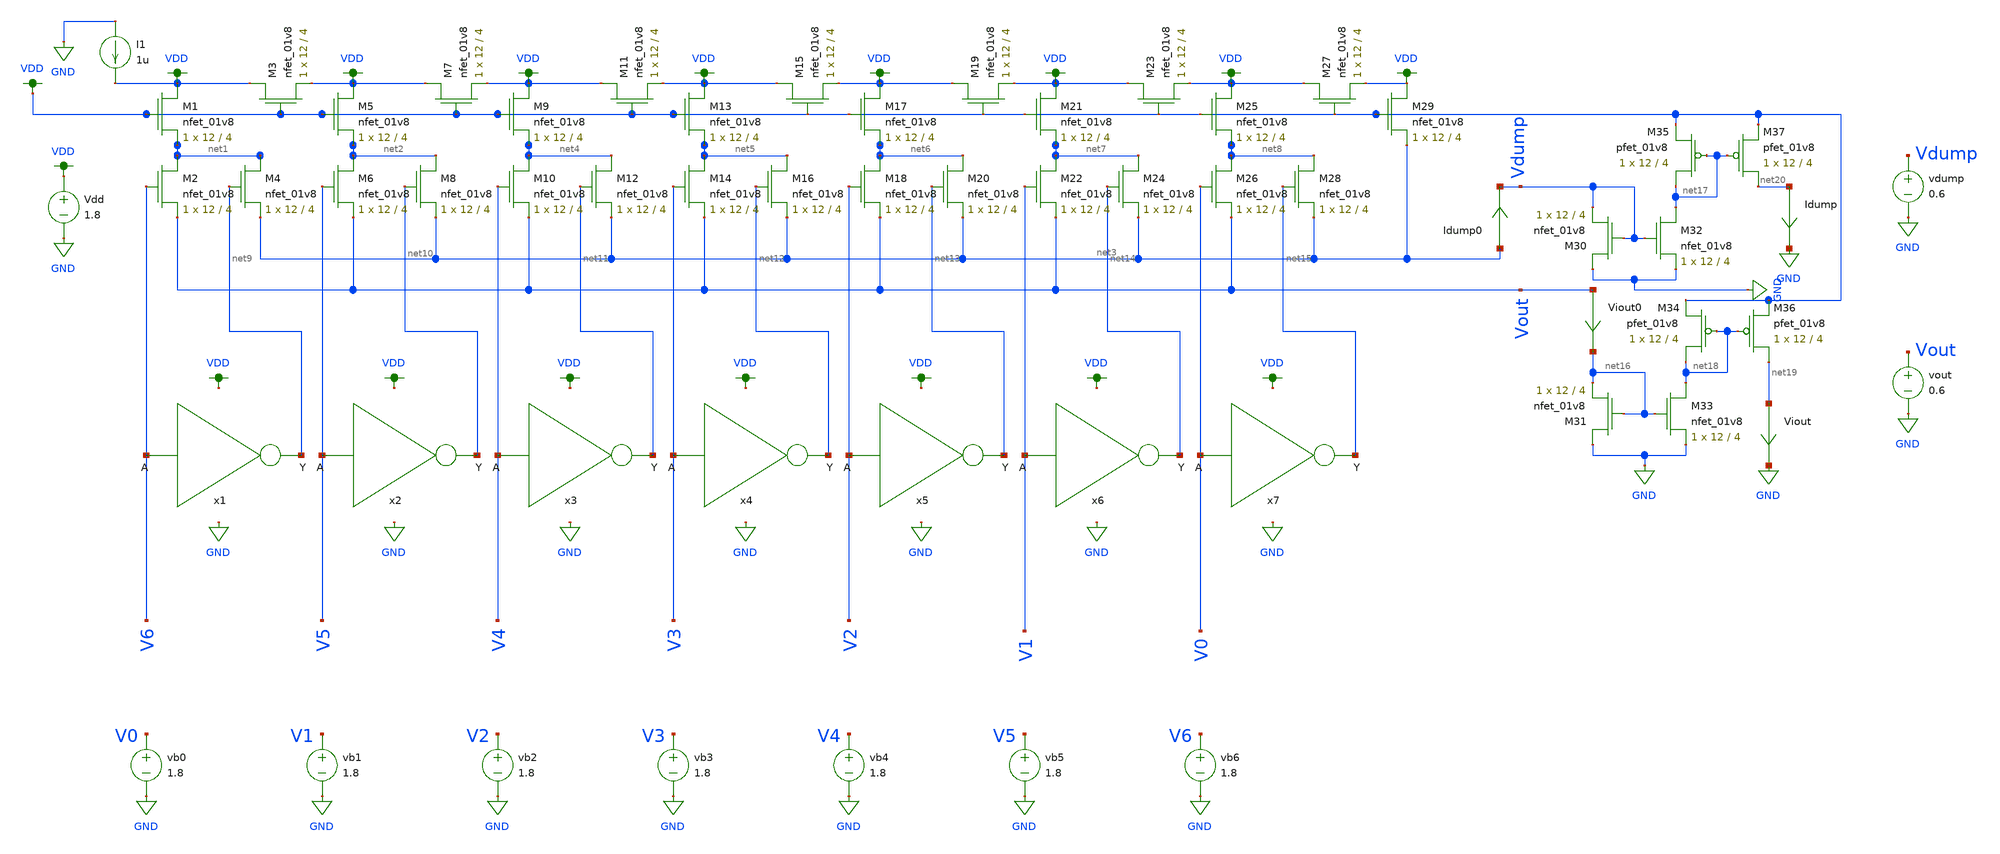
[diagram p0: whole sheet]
** sch_path: xschem/ladder_dac_simulation.sch
**.subckt ladder_dac_simulation
XM1 VDD VDD net1 GND sky130_fd_pr__nfet_01v8 L=4 W=12 nf=1 ad='int((nf+1)/2) * W/nf * 0.29' as='int((nf+2)/2) * W/nf * 0.29'
+ pd='2*int((nf+1)/2) * (W/nf + 0.29)' ps='2*int((nf+2)/2) * (W/nf + 0.29)' nrd='0.29 / W' nrs='0.29 / W'
+ sa=0 sb=0 sd=0 mult=1 m=1
XM3 VDD VDD VDD GND sky130_fd_pr__nfet_01v8 L=4 W=12 nf=1 ad='int((nf+1)/2) * W/nf * 0.29' as='int((nf+2)/2) * W/nf * 0.29'
+ pd='2*int((nf+1)/2) * (W/nf + 0.29)' ps='2*int((nf+2)/2) * (W/nf + 0.29)' nrd='0.29 / W' nrs='0.29 / W'
+ sa=0 sb=0 sd=0 mult=1 m=1
XM5 VDD VDD net2 GND sky130_fd_pr__nfet_01v8 L=4 W=12 nf=1 ad='int((nf+1)/2) * W/nf * 0.29' as='int((nf+2)/2) * W/nf * 0.29'
+ pd='2*int((nf+1)/2) * (W/nf + 0.29)' ps='2*int((nf+2)/2) * (W/nf + 0.29)' nrd='0.29 / W' nrs='0.29 / W'
+ sa=0 sb=0 sd=0 mult=1 m=1
XM7 VDD VDD VDD GND sky130_fd_pr__nfet_01v8 L=4 W=12 nf=1 ad='int((nf+1)/2) * W/nf * 0.29' as='int((nf+2)/2) * W/nf * 0.29'
+ pd='2*int((nf+1)/2) * (W/nf + 0.29)' ps='2*int((nf+2)/2) * (W/nf + 0.29)' nrd='0.29 / W' nrs='0.29 / W'
+ sa=0 sb=0 sd=0 mult=1 m=1
XM6 net2 V5 Vout GND sky130_fd_pr__nfet_01v8 L=4 W=12 nf=1 ad='int((nf+1)/2) * W/nf * 0.29' as='int((nf+2)/2) * W/nf * 0.29'
+ pd='2*int((nf+1)/2) * (W/nf + 0.29)' ps='2*int((nf+2)/2) * (W/nf + 0.29)' nrd='0.29 / W' nrs='0.29 / W'
+ sa=0 sb=0 sd=0 mult=1 m=1
XM8 net2 net10 net3 GND sky130_fd_pr__nfet_01v8 L=4 W=12 nf=1 ad='int((nf+1)/2) * W/nf * 0.29' as='int((nf+2)/2) * W/nf * 0.29'
+ pd='2*int((nf+1)/2) * (W/nf + 0.29)' ps='2*int((nf+2)/2) * (W/nf + 0.29)' nrd='0.29 / W' nrs='0.29 / W'
+ sa=0 sb=0 sd=0 mult=1 m=1
XM2 net1 V6 Vout GND sky130_fd_pr__nfet_01v8 L=4 W=12 nf=1 ad='int((nf+1)/2) * W/nf * 0.29' as='int((nf+2)/2) * W/nf * 0.29'
+ pd='2*int((nf+1)/2) * (W/nf + 0.29)' ps='2*int((nf+2)/2) * (W/nf + 0.29)' nrd='0.29 / W' nrs='0.29 / W'
+ sa=0 sb=0 sd=0 mult=1 m=1
XM4 net1 net9 net3 GND sky130_fd_pr__nfet_01v8 L=4 W=12 nf=1 ad='int((nf+1)/2) * W/nf * 0.29' as='int((nf+2)/2) * W/nf * 0.29'
+ pd='2*int((nf+1)/2) * (W/nf + 0.29)' ps='2*int((nf+2)/2) * (W/nf + 0.29)' nrd='0.29 / W' nrs='0.29 / W'
+ sa=0 sb=0 sd=0 mult=1 m=1
XM9 VDD VDD net4 GND sky130_fd_pr__nfet_01v8 L=4 W=12 nf=1 ad='int((nf+1)/2) * W/nf * 0.29' as='int((nf+2)/2) * W/nf * 0.29'
+ pd='2*int((nf+1)/2) * (W/nf + 0.29)' ps='2*int((nf+2)/2) * (W/nf + 0.29)' nrd='0.29 / W' nrs='0.29 / W'
+ sa=0 sb=0 sd=0 mult=1 m=1
XM11 VDD VDD VDD GND sky130_fd_pr__nfet_01v8 L=4 W=12 nf=1 ad='int((nf+1)/2) * W/nf * 0.29' as='int((nf+2)/2) * W/nf * 0.29'
+ pd='2*int((nf+1)/2) * (W/nf + 0.29)' ps='2*int((nf+2)/2) * (W/nf + 0.29)' nrd='0.29 / W' nrs='0.29 / W'
+ sa=0 sb=0 sd=0 mult=1 m=1
XM10 net4 V4 Vout GND sky130_fd_pr__nfet_01v8 L=4 W=12 nf=1 ad='int((nf+1)/2) * W/nf * 0.29' as='int((nf+2)/2) * W/nf * 0.29'
+ pd='2*int((nf+1)/2) * (W/nf + 0.29)' ps='2*int((nf+2)/2) * (W/nf + 0.29)' nrd='0.29 / W' nrs='0.29 / W'
+ sa=0 sb=0 sd=0 mult=1 m=1
XM12 net4 net11 net3 GND sky130_fd_pr__nfet_01v8 L=4 W=12 nf=1 ad='int((nf+1)/2) * W/nf * 0.29' as='int((nf+2)/2) * W/nf * 0.29'
+ pd='2*int((nf+1)/2) * (W/nf + 0.29)' ps='2*int((nf+2)/2) * (W/nf + 0.29)' nrd='0.29 / W' nrs='0.29 / W'
+ sa=0 sb=0 sd=0 mult=1 m=1
XM13 VDD VDD net5 GND sky130_fd_pr__nfet_01v8 L=4 W=12 nf=1 ad='int((nf+1)/2) * W/nf * 0.29' as='int((nf+2)/2) * W/nf * 0.29'
+ pd='2*int((nf+1)/2) * (W/nf + 0.29)' ps='2*int((nf+2)/2) * (W/nf + 0.29)' nrd='0.29 / W' nrs='0.29 / W'
+ sa=0 sb=0 sd=0 mult=1 m=1
XM15 VDD VDD VDD GND sky130_fd_pr__nfet_01v8 L=4 W=12 nf=1 ad='int((nf+1)/2) * W/nf * 0.29' as='int((nf+2)/2) * W/nf * 0.29'
+ pd='2*int((nf+1)/2) * (W/nf + 0.29)' ps='2*int((nf+2)/2) * (W/nf + 0.29)' nrd='0.29 / W' nrs='0.29 / W'
+ sa=0 sb=0 sd=0 mult=1 m=1
XM14 net5 V3 Vout GND sky130_fd_pr__nfet_01v8 L=4 W=12 nf=1 ad='int((nf+1)/2) * W/nf * 0.29' as='int((nf+2)/2) * W/nf * 0.29'
+ pd='2*int((nf+1)/2) * (W/nf + 0.29)' ps='2*int((nf+2)/2) * (W/nf + 0.29)' nrd='0.29 / W' nrs='0.29 / W'
+ sa=0 sb=0 sd=0 mult=1 m=1
XM16 net5 net12 net3 GND sky130_fd_pr__nfet_01v8 L=4 W=12 nf=1 ad='int((nf+1)/2) * W/nf * 0.29' as='int((nf+2)/2) * W/nf * 0.29'
+ pd='2*int((nf+1)/2) * (W/nf + 0.29)' ps='2*int((nf+2)/2) * (W/nf + 0.29)' nrd='0.29 / W' nrs='0.29 / W'
+ sa=0 sb=0 sd=0 mult=1 m=1
XM17 VDD VDD net6 GND sky130_fd_pr__nfet_01v8 L=4 W=12 nf=1 ad='int((nf+1)/2) * W/nf * 0.29' as='int((nf+2)/2) * W/nf * 0.29'
+ pd='2*int((nf+1)/2) * (W/nf + 0.29)' ps='2*int((nf+2)/2) * (W/nf + 0.29)' nrd='0.29 / W' nrs='0.29 / W'
+ sa=0 sb=0 sd=0 mult=1 m=1
XM19 VDD VDD VDD GND sky130_fd_pr__nfet_01v8 L=4 W=12 nf=1 ad='int((nf+1)/2) * W/nf * 0.29' as='int((nf+2)/2) * W/nf * 0.29'
+ pd='2*int((nf+1)/2) * (W/nf + 0.29)' ps='2*int((nf+2)/2) * (W/nf + 0.29)' nrd='0.29 / W' nrs='0.29 / W'
+ sa=0 sb=0 sd=0 mult=1 m=1
XM18 net6 V2 Vout GND sky130_fd_pr__nfet_01v8 L=4 W=12 nf=1 ad='int((nf+1)/2) * W/nf * 0.29' as='int((nf+2)/2) * W/nf * 0.29'
+ pd='2*int((nf+1)/2) * (W/nf + 0.29)' ps='2*int((nf+2)/2) * (W/nf + 0.29)' nrd='0.29 / W' nrs='0.29 / W'
+ sa=0 sb=0 sd=0 mult=1 m=1
XM20 net6 net13 net3 GND sky130_fd_pr__nfet_01v8 L=4 W=12 nf=1 ad='int((nf+1)/2) * W/nf * 0.29' as='int((nf+2)/2) * W/nf * 0.29'
+ pd='2*int((nf+1)/2) * (W/nf + 0.29)' ps='2*int((nf+2)/2) * (W/nf + 0.29)' nrd='0.29 / W' nrs='0.29 / W'
+ sa=0 sb=0 sd=0 mult=1 m=1
XM21 VDD VDD net7 GND sky130_fd_pr__nfet_01v8 L=4 W=12 nf=1 ad='int((nf+1)/2) * W/nf * 0.29' as='int((nf+2)/2) * W/nf * 0.29'
+ pd='2*int((nf+1)/2) * (W/nf + 0.29)' ps='2*int((nf+2)/2) * (W/nf + 0.29)' nrd='0.29 / W' nrs='0.29 / W'
+ sa=0 sb=0 sd=0 mult=1 m=1
XM23 VDD VDD VDD GND sky130_fd_pr__nfet_01v8 L=4 W=12 nf=1 ad='int((nf+1)/2) * W/nf * 0.29' as='int((nf+2)/2) * W/nf * 0.29'
+ pd='2*int((nf+1)/2) * (W/nf + 0.29)' ps='2*int((nf+2)/2) * (W/nf + 0.29)' nrd='0.29 / W' nrs='0.29 / W'
+ sa=0 sb=0 sd=0 mult=1 m=1
XM22 net7 V1 Vout GND sky130_fd_pr__nfet_01v8 L=4 W=12 nf=1 ad='int((nf+1)/2) * W/nf * 0.29' as='int((nf+2)/2) * W/nf * 0.29'
+ pd='2*int((nf+1)/2) * (W/nf + 0.29)' ps='2*int((nf+2)/2) * (W/nf + 0.29)' nrd='0.29 / W' nrs='0.29 / W'
+ sa=0 sb=0 sd=0 mult=1 m=1
XM24 net7 net14 net3 GND sky130_fd_pr__nfet_01v8 L=4 W=12 nf=1 ad='int((nf+1)/2) * W/nf * 0.29' as='int((nf+2)/2) * W/nf * 0.29'
+ pd='2*int((nf+1)/2) * (W/nf + 0.29)' ps='2*int((nf+2)/2) * (W/nf + 0.29)' nrd='0.29 / W' nrs='0.29 / W'
+ sa=0 sb=0 sd=0 mult=1 m=1
XM25 VDD VDD net8 GND sky130_fd_pr__nfet_01v8 L=4 W=12 nf=1 ad='int((nf+1)/2) * W/nf * 0.29' as='int((nf+2)/2) * W/nf * 0.29'
+ pd='2*int((nf+1)/2) * (W/nf + 0.29)' ps='2*int((nf+2)/2) * (W/nf + 0.29)' nrd='0.29 / W' nrs='0.29 / W'
+ sa=0 sb=0 sd=0 mult=1 m=1
XM27 VDD VDD VDD GND sky130_fd_pr__nfet_01v8 L=4 W=12 nf=1 ad='int((nf+1)/2) * W/nf * 0.29' as='int((nf+2)/2) * W/nf * 0.29'
+ pd='2*int((nf+1)/2) * (W/nf + 0.29)' ps='2*int((nf+2)/2) * (W/nf + 0.29)' nrd='0.29 / W' nrs='0.29 / W'
+ sa=0 sb=0 sd=0 mult=1 m=1
XM26 net8 V0 Vout GND sky130_fd_pr__nfet_01v8 L=4 W=12 nf=1 ad='int((nf+1)/2) * W/nf * 0.29' as='int((nf+2)/2) * W/nf * 0.29'
+ pd='2*int((nf+1)/2) * (W/nf + 0.29)' ps='2*int((nf+2)/2) * (W/nf + 0.29)' nrd='0.29 / W' nrs='0.29 / W'
+ sa=0 sb=0 sd=0 mult=1 m=1
XM28 net8 net15 net3 GND sky130_fd_pr__nfet_01v8 L=4 W=12 nf=1 ad='int((nf+1)/2) * W/nf * 0.29' as='int((nf+2)/2) * W/nf * 0.29'
+ pd='2*int((nf+1)/2) * (W/nf + 0.29)' ps='2*int((nf+2)/2) * (W/nf + 0.29)' nrd='0.29 / W' nrs='0.29 / W'
+ sa=0 sb=0 sd=0 mult=1 m=1
XM29 VDD VDD net3 GND sky130_fd_pr__nfet_01v8 L=4 W=12 nf=1 ad='int((nf+1)/2) * W/nf * 0.29' as='int((nf+2)/2) * W/nf * 0.29'
+ pd='2*int((nf+1)/2) * (W/nf + 0.29)' ps='2*int((nf+2)/2) * (W/nf + 0.29)' nrd='0.29 / W' nrs='0.29 / W'
+ sa=0 sb=0 sd=0 mult=1 m=1
x1 net9 V6 inverter
x2 net10 V5 inverter
x3 net11 V4 inverter
x4 net12 V3 inverter
x5 net13 V2 inverter
x6 net14 V1 inverter
x7 net15 V0 inverter
XM30 GND Vdump Vdump GND sky130_fd_pr__nfet_01v8 L=4 W=12 nf=1 ad='int((nf+1)/2) * W/nf * 0.29' as='int((nf+2)/2) * W/nf * 0.29'
+ pd='2*int((nf+1)/2) * (W/nf + 0.29)' ps='2*int((nf+2)/2) * (W/nf + 0.29)' nrd='0.29 / W' nrs='0.29 / W'
+ sa=0 sb=0 sd=0 mult=1 m=1
XM31 GND net16 net16 GND sky130_fd_pr__nfet_01v8 L=4 W=12 nf=1 ad='int((nf+1)/2) * W/nf * 0.29' as='int((nf+2)/2) * W/nf * 0.29'
+ pd='2*int((nf+1)/2) * (W/nf + 0.29)' ps='2*int((nf+2)/2) * (W/nf + 0.29)' nrd='0.29 / W' nrs='0.29 / W'
+ sa=0 sb=0 sd=0 mult=1 m=1
XM32 net17 Vdump GND GND sky130_fd_pr__nfet_01v8 L=4 W=12 nf=1 ad='int((nf+1)/2) * W/nf * 0.29' as='int((nf+2)/2) * W/nf * 0.29'
+ pd='2*int((nf+1)/2) * (W/nf + 0.29)' ps='2*int((nf+2)/2) * (W/nf + 0.29)' nrd='0.29 / W' nrs='0.29 / W'
+ sa=0 sb=0 sd=0 mult=1 m=1
XM33 net18 net16 GND GND sky130_fd_pr__nfet_01v8 L=4 W=12 nf=1 ad='int((nf+1)/2) * W/nf * 0.29' as='int((nf+2)/2) * W/nf * 0.29'
+ pd='2*int((nf+1)/2) * (W/nf + 0.29)' ps='2*int((nf+2)/2) * (W/nf + 0.29)' nrd='0.29 / W' nrs='0.29 / W'
+ sa=0 sb=0 sd=0 mult=1 m=1
XM35 net17 net17 VDD VDD sky130_fd_pr__pfet_01v8 L=4 W=12 nf=1 ad='int((nf+1)/2) * W/nf * 0.29' as='int((nf+2)/2) * W/nf * 0.29'
+ pd='2*int((nf+1)/2) * (W/nf + 0.29)' ps='2*int((nf+2)/2) * (W/nf + 0.29)' nrd='0.29 / W' nrs='0.29 / W'
+ sa=0 sb=0 sd=0 mult=1 m=1
XM37 net20 net17 VDD VDD sky130_fd_pr__pfet_01v8 L=4 W=12 nf=1 ad='int((nf+1)/2) * W/nf * 0.29' as='int((nf+2)/2) * W/nf * 0.29'
+ pd='2*int((nf+1)/2) * (W/nf + 0.29)' ps='2*int((nf+2)/2) * (W/nf + 0.29)' nrd='0.29 / W' nrs='0.29 / W'
+ sa=0 sb=0 sd=0 mult=1 m=1
XM34 net18 net18 VDD VDD sky130_fd_pr__pfet_01v8 L=4 W=12 nf=1 ad='int((nf+1)/2) * W/nf * 0.29' as='int((nf+2)/2) * W/nf * 0.29'
+ pd='2*int((nf+1)/2) * (W/nf + 0.29)' ps='2*int((nf+2)/2) * (W/nf + 0.29)' nrd='0.29 / W' nrs='0.29 / W'
+ sa=0 sb=0 sd=0 mult=1 m=1
XM36 net19 net18 VDD VDD sky130_fd_pr__pfet_01v8 L=4 W=12 nf=1 ad='int((nf+1)/2) * W/nf * 0.29' as='int((nf+2)/2) * W/nf * 0.29'
+ pd='2*int((nf+1)/2) * (W/nf + 0.29)' ps='2*int((nf+2)/2) * (W/nf + 0.29)' nrd='0.29 / W' nrs='0.29 / W'
+ sa=0 sb=0 sd=0 mult=1 m=1
I1 GND VDD 1u
Vdd VDD GND 1.8
vb0 V0 GND 1.8
vb1 V1 GND 1.8
vb2 V2 GND 1.8
vb3 V3 GND 1.8
vb4 V4 GND 1.8
vb5 V5 GND 1.8
vb6 V6 GND 1.8
vdump Vdump GND 0.6
vout Vout GND 0.6
Idump net20 GND 0
.save i(idump)
Viout net19 GND 0
.save i(viout)
Idump0 net3 Vdump 0
.save i(idump0)
Viout0 Vout net16 0
.save i(viout0)
**** begin user architecture code

.option wnflag=1
.param MC_SWITCH=0.0
.lib ~/skywater/skywater-pdk/libraries/sky130_fd_pr_ngspice/latest/models/sky130.lib.spice tt



.control
  set wr_vecnames
  set wr_singlescale
  let code = 0
  while code < 128
    if code eq 0
      let b0 = 0
    else
      let b0 = code % 2
    end
    if floor(code / 2) eq 0
      let b1 = 0
    else
      let b1 = floor(code / 2) % 2
    end
    if floor(code / 4) eq 0
      let b2 = 0
    else
      let b2 = floor(code / 4) % 2
    end
    if floor(code / 8) eq 0
      let b3 = 0
    else
      let b3 = floor(code / 8) % 2
    end
    if floor(code / 16) eq 0
      let b4 = 0
    else
      let b4 = floor(code / 16) % 2
    end
    if floor(code / 32) eq 0
      let b5 = 0
    else
      let b5 = floor(code / 32) % 2
    end
    if floor(code / 64) eq 0
      let b6 = 0
    else
      let b6 = floor(code / 64) % 2
    end
    alter Vb0 1.8*$&b0
    alter Vb1 1.8*$&b1
    alter Vb2 1.8*$&b2
    alter Vb3 1.8*$&b3
    alter Vb4 1.8*$&b4
    alter Vb5 1.8*$&b5
    alter Vb6 1.8*$&b6
    save all
    op
    wrdata ~/Documents/DAC-VLSI/simulation_results/ladder_dac_simulation_andrew.txt v(b0) v(b1)
+ v(b2) v(b3) v(b4) v(b5) v(b6) i(Viout)
    if code eq 0
      set appendwrite
      set wr_vecnames = FALSE
    end
    let code = code + 1
  end
  quit
.endc

**** end user architecture code
**.ends

* expanding   symbol:  ./inverter.sym # of pins=2
** sym_path: xschem/inverter.sym
** sch_path: xschem/inverter.sch
.subckt inverter Y A
*.ipin A
*.opin Y
XM1 Y A VDD VDD sky130_fd_pr__pfet_01v8 L=0.15 W=1 nf=1 ad='int((nf+1)/2) * W/nf * 0.29' as='int((nf+2)/2) * W/nf * 0.29'
+ pd='2*int((nf+1)/2) * (W/nf + 0.29)' ps='2*int((nf+2)/2) * (W/nf + 0.29)' nrd='0.29 / W' nrs='0.29 / W'
+ sa=0 sb=0 sd=0 mult=1 m=1
XM2 Y A GND GND sky130_fd_pr__nfet_01v8 L=0.15 W=1 nf=1 ad='int((nf+1)/2) * W/nf * 0.29' as='int((nf+2)/2) * W/nf * 0.29'
+ pd='2*int((nf+1)/2) * (W/nf + 0.29)' ps='2*int((nf+2)/2) * (W/nf + 0.29)' nrd='0.29 / W' nrs='0.29 / W'
+ sa=0 sb=0 sd=0 mult=1 m=1
.ends

.GLOBAL VDD
.GLOBAL GND
.end
